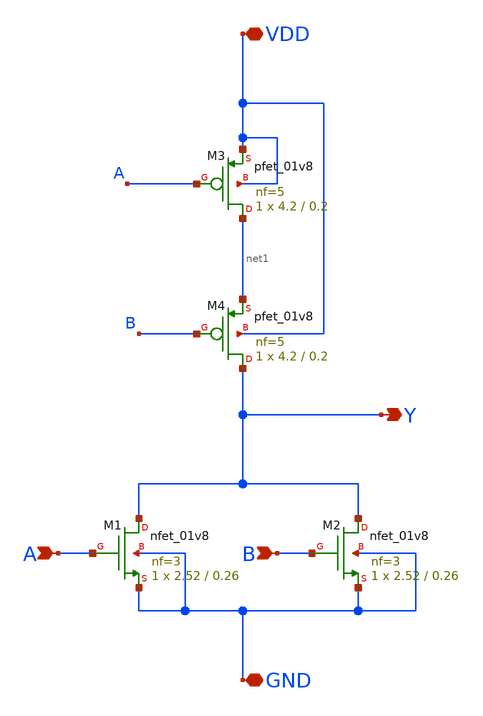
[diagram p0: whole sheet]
** sch_path: cells/NOR2X4/schematic/nor2x4.sch
**.subckt nor2x4 A B VDD GND Y
*.ipin A
*.ipin B
*.iopin VDD
*.iopin GND
*.opin Y
XM1 Y A GND GND sky130_fd_pr__nfet_01v8 L=0.26 W=2.52 nf=3 ad='int((3 + 1)/2) * 2.52 / 3 * 0.29' as='int((3 + 2)/2) * 2.52 / 3 * 0.29'
+ pd='2*int((3 + 1)/2) * (2.52 / 3 + 0.29)' ps='2*int((3 + 2)/2) * (2.52 / 3 + 0.29)' nrd='0.29 / 2.52 '
+ nrs='0.29 / 2.52 ' sa=0 sb=0 sd=0 mult=1 m=1
XM3 net1 A VDD VDD sky130_fd_pr__pfet_01v8 L=0.2 W=4.2 nf=5 ad='int((5 + 1)/2) * 4.2 / 5 * 0.29' as='int((5 + 2)/2) * 4.2 / 5 * 0.29'
+ pd='2*int((5 + 1)/2) * (4.2 / 5 + 0.29)' ps='2*int((5 + 2)/2) * (4.2 / 5 + 0.29)' nrd='0.29 / 4.2 ' nrs='0.29 / 4.2 '
+ sa=0 sb=0 sd=0 mult=1 m=1
XM4 Y B net1 VDD sky130_fd_pr__pfet_01v8 L=0.2 W=4.2 nf=5 ad='int((5 + 1)/2) * 4.2 / 5 * 0.29' as='int((5 + 2)/2) * 4.2 / 5 * 0.29'
+ pd='2*int((5 + 1)/2) * (4.2 / 5 + 0.29)' ps='2*int((5 + 2)/2) * (4.2 / 5 + 0.29)' nrd='0.29 / 4.2 ' nrs='0.29 / 4.2 '
+ sa=0 sb=0 sd=0 mult=1 m=1
XM2 Y B GND GND sky130_fd_pr__nfet_01v8 L=0.26 W=2.52 nf=3 ad='int((3 + 1)/2) * 2.52 / 3 * 0.29' as='int((3 + 2)/2) * 2.52 / 3 * 0.29'
+ pd='2*int((3 + 1)/2) * (2.52 / 3 + 0.29)' ps='2*int((3 + 2)/2) * (2.52 / 3 + 0.29)' nrd='0.29 / 2.52 '
+ nrs='0.29 / 2.52 ' sa=0 sb=0 sd=0 mult=1 m=1
**.ends
.end
